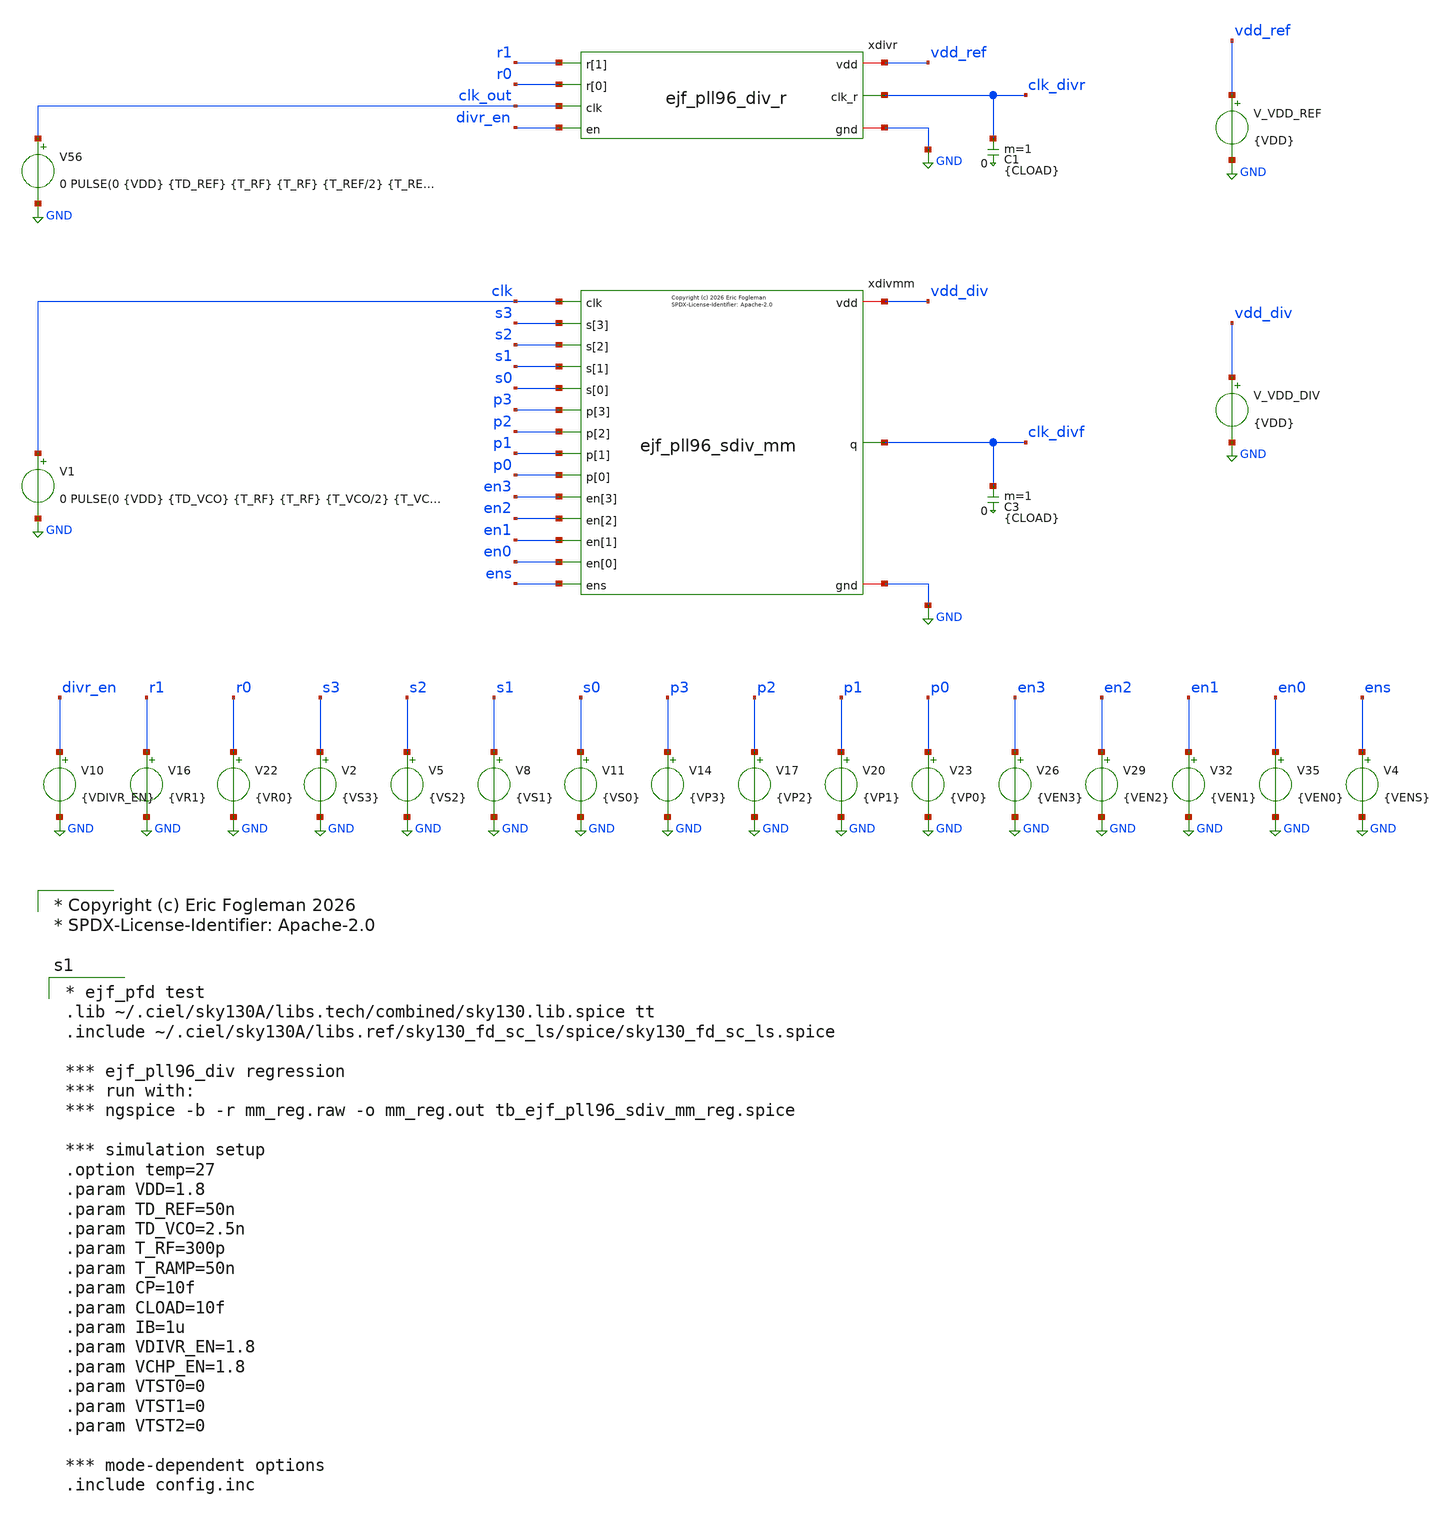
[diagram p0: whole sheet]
** sch_path: xschem/tb_ejf_pll96_sdiv_mm_reg.sch
* xschem/ejf_pll96_sdiv23.sym:
* Copyright (c) 2026 Eric Fogleman

* Copyright (c) Eric Fogleman 2026
* SPDX-License-Identifier: Apache-2.0

**.subckt tb_ejf_pll96_sdiv_mm_reg
V1 clk GND 0 PULSE(0 {VDD} {TD_VCO} {T_RF} {T_RF} {T_VCO/2} {T_VCO})
V_VDD_DIV vdd_div GND {VDD}
.save i(v_vdd_div)
V2 s3 GND {VS3}
V5 s2 GND {VS2}
V8 s1 GND {VS1}
V11 s0 GND {VS0}
V14 p3 GND {VP3}
V17 p2 GND {VP2}
V20 p1 GND {VP1}
V23 p0 GND {VP0}
V26 en3 GND {VEN3}
V29 en2 GND {VEN2}
V32 en1 GND {VEN1}
V35 en0 GND {VEN0}
V4 ens GND {VENS}
V10 divr_en GND {VDIVR_EN}
V16 r1 GND {VR1}
V22 r0 GND {VR0}
xdivmm p3 clk p2 p1 clk_divf p0 en3 en2 en1 s3 s2 s1 s0 vdd_div GND en0 ens ejf_pll96_sdiv_mm
C3 clk_divf 0 {CLOAD} m=1
xdivr divr_en clk_out clk_divr r1 vdd_ref GND r0 ejf_pll96_div_r
C1 clk_divr 0 {CLOAD} m=1
V_VDD_REF vdd_ref GND {VDD}
.save i(v_vdd_ref)
V56 clk_out GND 0 PULSE(0 {VDD} {TD_REF} {T_RF} {T_RF} {T_REF/2} {T_REF})
**** begin user architecture code

* ejf_pfd test
.lib ~/.ciel/sky130A/libs.tech/combined/sky130.lib.spice tt
.include ~/.ciel/sky130A/libs.ref/sky130_fd_sc_ls/spice/sky130_fd_sc_ls.spice

*** ejf_pll96_div regression
*** run with:
*** ngspice -b -r mm_reg.raw -o mm_reg.out tb_ejf_pll96_sdiv_mm_reg.spice

*** simulation setup
.option temp=27
.param VDD=1.8
.param TD_REF=50n
.param TD_VCO=2.5n
.param T_RF=300p
.param T_RAMP=50n
.param CP=10f
.param CLOAD=10f
.param IB=1u
.param VDIVR_EN=1.8
.param VCHP_EN=1.8
.param VTST0=0
.param VTST1=0
.param VTST2=0

*** mode-dependent options
.include config.inc



* Run transient
* default reltol=1e-3 vntol=1e-6 abstol=1e-12
.options  reltol=1e-4 vntol=1e-7 abstol=1e-13
*.options klu
.control
   save i(v_vdd_ref) i(v_vdd_div)
   save clk clk_out clk_divr clk_divf
   save xdivmm.clk_div23 xdivmm.mc
   save xdivmm.xp.q3 xdivmm.xp.q2 xdivmm.xp.q1 xdivmm.xp.q0 xdivmm.xp.q3_or_dis xdivmm.xp.q2_or_dis
+ xdivmm.xp.q1_or_dis xdivmm.xp.q0_or_dis
   save xdivmm.q
   save xdivmm.xn.q1 xdivmm.xn.d2
   tran 1n 2u
   write tb_ejf_pll96_sdiv_mm_reg.raw
   meas tran idd_ref avg i(v_vdd_ref) from=800n to=2u
   meas tran idd_div avg i(v_vdd_div) from=800n to=2u
   meas tran T_CLK_DIVF trig v(clk_divf) val=0.9 rise=1 td=800n targ v(clk_divf) val=0.9 rise=2
+ td=800n
   print 1/T_CLK_DIVF
   meas tran T_CLK_DIVR trig v(clk_divr) val=0.9 rise=1 td=800n targ v(clk_divr) val=0.9 rise=2
+ td=800n
   print 1/T_CLK_DIVR
   * plot clk_divr clk_divf
.endc
.end

**** end user architecture code
**.ends

* expanding   symbol:  ejf_pll96_sdiv_mm.sym # of pins=17
** sym_path: xschem/ejf_pll96_sdiv_mm.sym
** sch_path: xschem/ejf_pll96_sdiv_mm.sch
.subckt ejf_pll96_sdiv_mm p[3] clk p[2] p[1] q p[0] en[3] en[2] en[1] s[3] s[2] s[1] s[0] vdd gnd
+ en[0] ens
*.iopin gnd
*.ipin clk
*.opin q
*.iopin vdd
*.ipin p[3]
*.ipin p[2]
*.ipin p[1]
*.ipin p[0]
*.ipin en[3]
*.ipin en[2]
*.ipin en[1]
*.ipin s[0]
*.ipin s[1]
*.ipin s[2]
*.ipin s[3]
*.ipin ens
*.ipin en[0]
xn clk_div23 clk mc vdd gnd vdd ejf_pll96_sdiv23
xp clk_div23 p[0] en[1] p[1] ld en[2] p[2] en[3] p[3] vdd gnd en[0] ejf_pll96_sdiv_p
xs clk_div23 s[0] s[1] s[3] s[2] ld mc vdd gnd ens ejf_pll96_sdiv_s
**** begin user architecture code

* Copyright (c) Eric Fogleman 2026
* SPDX-License-Identifier: Apache-2.0

**** end user architecture code
x1 clk ld gnd gnd vdd vdd q sky130_fd_sc_ls__dfxtp_2
.ends


* expanding   symbol:  ejf_pll96_div_r.sym # of pins=7
** sym_path: xschem/ejf_pll96_div_r.sym
** sch_path: xschem/ejf_pll96_div_r.sch
.subckt ejf_pll96_div_r en clk clk_r r[1] vdd gnd r[0]
*.ipin clk
*.iopin vdd
*.iopin gnd
*.ipin en
*.ipin r[0]
*.ipin r[1]
*.opin clk_r
xdff0 net6 net1 en gnd gnd vdd vdd net2 net1 sky130_fd_sc_ls__dfrbp_2
x1 net6 net2 r[0] gnd gnd vdd vdd net4 sky130_fd_sc_ls__mux2_2
x2 net4 net5 r[1] gnd gnd vdd vdd clk_r sky130_fd_sc_ls__mux2_2
xdff1 net2 net3 en gnd gnd vdd vdd net5 net3 sky130_fd_sc_ls__dfrbp_2
x3 clk en gnd gnd vdd vdd net6 sky130_fd_sc_ls__and2_2
.ends


* expanding   symbol:  ejf_pll96_sdiv23.sym # of pins=6
** sym_path: xschem/ejf_pll96_sdiv23.sym
** sch_path: xschem/ejf_pll96_sdiv23.sch
.subckt ejf_pll96_sdiv23 q2 clk mc vdd gnd en
*.ipin clk
*.ipin mc
*.opin q2
*.iopin vdd
*.iopin gnd
*.ipin en
x3 q1 mc q2_b gnd gnd vdd vdd d2 sky130_fd_sc_ls__o21a_1
**** begin user architecture code

* Copyright (c) Eric Fogleman 2026
* SPDX-License-Identifier: Apache-2.0

**** end user architecture code
x1 clk q2_b en gnd gnd vdd vdd q1 sky130_fd_sc_ls__edfxtp_1
x2 clk d2 en gnd gnd vdd vdd q2 q2_b sky130_fd_sc_ls__edfxbp_1
.ends


* expanding   symbol:  ejf_pll96_sdiv_p.sym # of pins=12
** sym_path: xschem/ejf_pll96_sdiv_p.sym
** sch_path: xschem/ejf_pll96_sdiv_p.sch
.subckt ejf_pll96_sdiv_p clk p[0] en[1] p[1] q en[2] p[2] en[3] p[3] vdd gnd en[0]
*.iopin vdd
*.iopin gnd
*.ipin clk
*.ipin p[1]
*.ipin p[2]
*.ipin p[3]
*.ipin en[3]
*.ipin en[2]
*.opin q
*.ipin en[1]
*.ipin p[0]
*.ipin en[0]
**** begin user architecture code

* Copyright (c) Eric Fogleman 2025
* SPDX-License-Identifier: Apache-2.0

**** end user architecture code
x5 q0 clk p[0] vdd gnd en[0] ejf_pll96_sdiv23
x8 q1 clk p[1] vdd gnd net2 ejf_pll96_sdiv23
x9 q0 en[1] gnd gnd vdd vdd net2 sky130_fd_sc_ls__and2_1
x10 q2 clk p[2] vdd gnd net3 ejf_pll96_sdiv23
x11 net2 q1 en[2] gnd gnd vdd vdd net3 sky130_fd_sc_ls__and3_1
x12 q3 clk p[3] vdd gnd net1 ejf_pll96_sdiv23
x7 net3 q2 en[3] gnd gnd vdd vdd net1 sky130_fd_sc_ls__and3_1
x1 q3 net4 gnd gnd vdd vdd q3_or_dis sky130_fd_sc_ls__or2_1
x2 en[3] gnd gnd vdd vdd net4 sky130_fd_sc_ls__inv_1
x3 q2 net5 gnd gnd vdd vdd q2_or_dis sky130_fd_sc_ls__or2_1
x13 en[2] gnd gnd vdd vdd net5 sky130_fd_sc_ls__inv_1
x14 q1 net6 gnd gnd vdd vdd q1_or_dis sky130_fd_sc_ls__or2_1
x15 en[1] gnd gnd vdd vdd net6 sky130_fd_sc_ls__inv_1
x16 q0 net7 gnd gnd vdd vdd q0_or_dis sky130_fd_sc_ls__or2_1
x17 en[0] gnd gnd vdd vdd net7 sky130_fd_sc_ls__inv_1
x18 q0_or_dis q1_or_dis q2_or_dis q3_or_dis gnd gnd vdd vdd q sky130_fd_sc_ls__and4_2
.ends


* expanding   symbol:  ejf_pll96_sdiv_s.sym # of pins=10
** sym_path: xschem/ejf_pll96_sdiv_s.sym
** sch_path: xschem/ejf_pll96_sdiv_s.sch
.subckt ejf_pll96_sdiv_s clk s[0] s[1] s[3] s[2] ld q vdd gnd en
*.ipin s[1]
*.ipin s[2]
*.ipin s[3]
*.ipin clk
*.opin q
*.ipin ld
*.ipin s[0]
*.ipin en
*.iopin vdd
*.iopin gnd
**** begin user architecture code

* Copyright (c) Eric Fogleman 2026
* SPDX-License-Identifier: Apache-2.0

**** end user architecture code
x3 q[3] q[2] q[1] q[0] gnd gnd vdd vdd tc sky130_fd_sc_ls__and4_2
x27 tc gnd gnd vdd vdd tc_b sky130_fd_sc_ls__inv_2
x2 clk net6 en[0] gnd gnd vdd vdd q[0] net1 sky130_fd_sc_ls__edfxbp_1
x1 net1 net10 ld_d2 gnd gnd vdd vdd net6 sky130_fd_sc_ls__mux2_1
x5 clk net7 en[1] gnd gnd vdd vdd q[1] net2 sky130_fd_sc_ls__edfxbp_1
x6 net2 net11 ld_d2 gnd gnd vdd vdd net7 sky130_fd_sc_ls__mux2_1
x8 clk net8 en[2] gnd gnd vdd vdd q[2] net3 sky130_fd_sc_ls__edfxbp_1
x9 net3 net12 ld_d2 gnd gnd vdd vdd net8 sky130_fd_sc_ls__mux2_1
x11 clk net9 net4 gnd gnd vdd vdd q[3] net5 sky130_fd_sc_ls__edfxbp_1
x12 net5 net13 ld_d2 gnd gnd vdd vdd net9 sky130_fd_sc_ls__mux2_1
x4 tc_b ld_d2 gnd gnd vdd vdd en[0] sky130_fd_sc_ls__or2_1
x16 s[0] gnd gnd vdd vdd net10 sky130_fd_sc_ls__inv_1
x20 en[0] q[0] ld_d2 gnd gnd vdd vdd en[1] sky130_fd_sc_ls__a21o_1
x7 en[1] q[1] ld_d2 gnd gnd vdd vdd en[2] sky130_fd_sc_ls__a21o_1
x10 en[2] q[2] ld_d2 gnd gnd vdd vdd net4 sky130_fd_sc_ls__a21o_1
x13 ld gnd gnd vdd vdd ld_d2 sky130_fd_sc_ls__buf_2
x17 s[1] gnd gnd vdd vdd net11 sky130_fd_sc_ls__inv_1
x18 s[2] gnd gnd vdd vdd net12 sky130_fd_sc_ls__inv_1
x19 s[3] gnd gnd vdd vdd net13 sky130_fd_sc_ls__inv_1
x14 tc_b en gnd gnd vdd vdd q sky130_fd_sc_ls__nand2_2
.ends

.GLOBAL GND
.end
